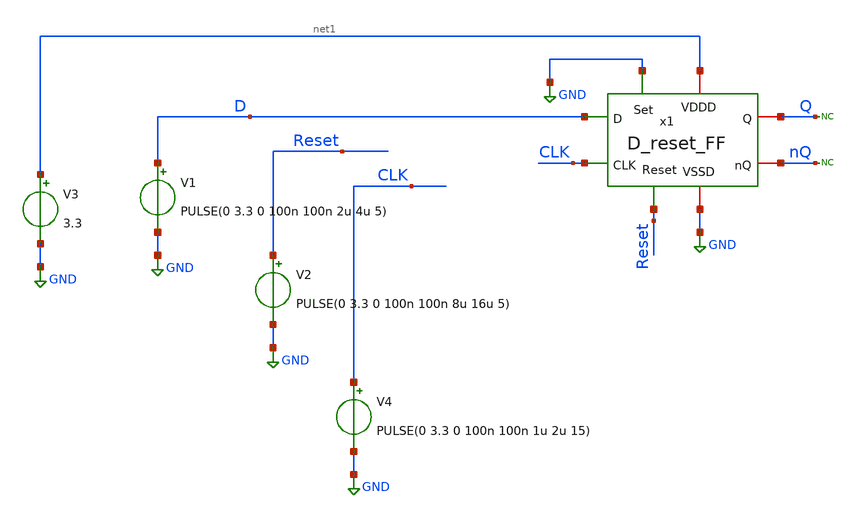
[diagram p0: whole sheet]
** sch_path: SAR_ADC/SAR_logic/xschem/D_reset_FF_tb.sch
**.subckt D_reset_FF_tb
* noconn Q
* noconn nQ
V3 net1 GND 3.3
V1 D GND PULSE(0 3.3 0 100n 100n 2u 4u 5)
V2 Reset GND PULSE(0 3.3 0 100n 100n 8u 16u 5)
V4 CLK GND PULSE(0 3.3 0 100n 100n 1u 2u 15)
x1 net1 Q CLK D nQ GND Reset GND D_reset_FF
**** begin user architecture code



*Parameters
.options TEMPS= 27.0

*Models
.include /home/gf180/Documents/gf180/pdk/gf180mcuD/libs.tech/ngspice/design.ngspice
.lib /home/gf180/Documents/gf180/pdk/gf180mcuD/libs.tech/ngspice/sm141064.ngspice typical
.lib /home/gf180/Documents/gf180/pdk/gf180mcuD/libs.tech/ngspice/smbb000149.ngspice typical


*Data to save
.save all

*Simulation
.control
tran 1n 30u
setplot dc1
plot V(D)+4 V(Reset)+8 V(CLK)+12 V(Q)
set filetype=ascii
write D_reset_FF_tb_tran.raw

reset
unset filetype
op
save all
write D_reset_FF_tb.raw

.endc
.end



**** end user architecture code
**.ends
.GLOBAL GND
.end
